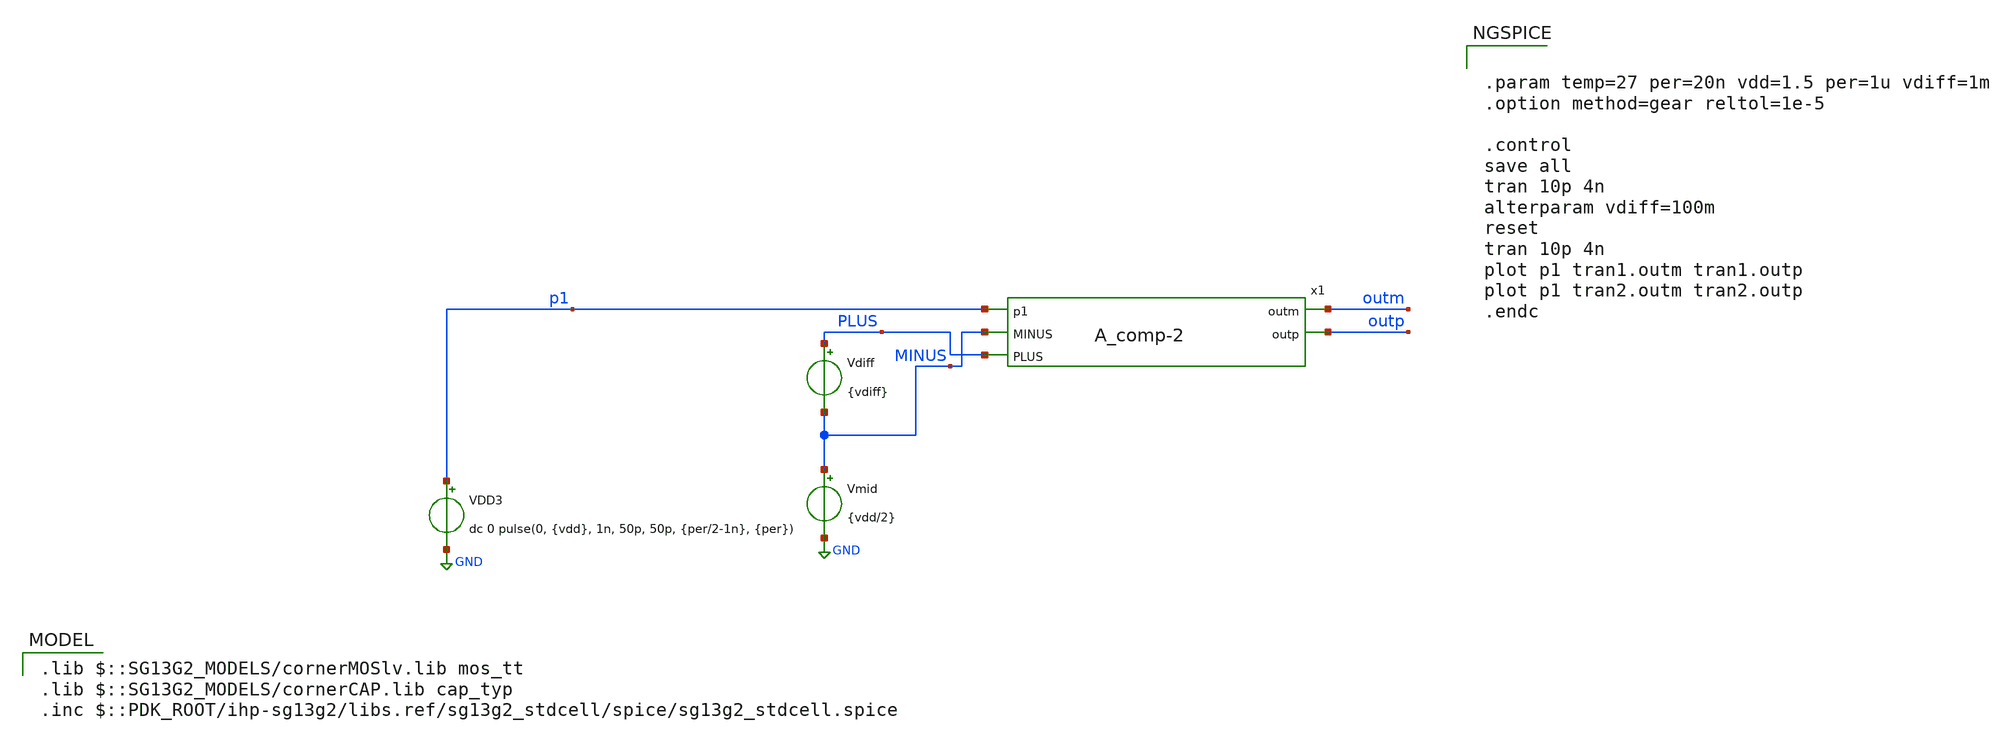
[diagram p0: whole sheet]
** sch_path: DSM/Schematics/Comparator_design_Sneha/tb_A_comp.sch
**.subckt tb_A_comp
Vdiff PLUS MINUS {vdiff}
Vmid MINUS GND {vdd/2}
VDD3 p1 GND dc 0 pulse(0, {vdd}, 1n, 50p, 50p, {per/2-1n}, {per})
x1 p1 outm outp MINUS PLUS A_comp-2
**** begin user architecture code


.param temp=27 per=20n vdd=1.5 per=1u vdiff=1m
.option method=gear reltol=1e-5

.control
save all
tran 10p 4n
alterparam vdiff=100m
reset
tran 10p 4n
plot p1 tran1.outm tran1.outp
plot p1 tran2.outm tran2.outp
.endc


 .lib $::SG13G2_MODELS/cornerMOSlv.lib mos_tt
.lib $::SG13G2_MODELS/cornerCAP.lib cap_typ
.inc $::PDK_ROOT/ihp-sg13g2/libs.ref/sg13g2_stdcell/spice/sg13g2_stdcell.spice

**** end user architecture code
**.ends
.GLOBAL GND
.end
